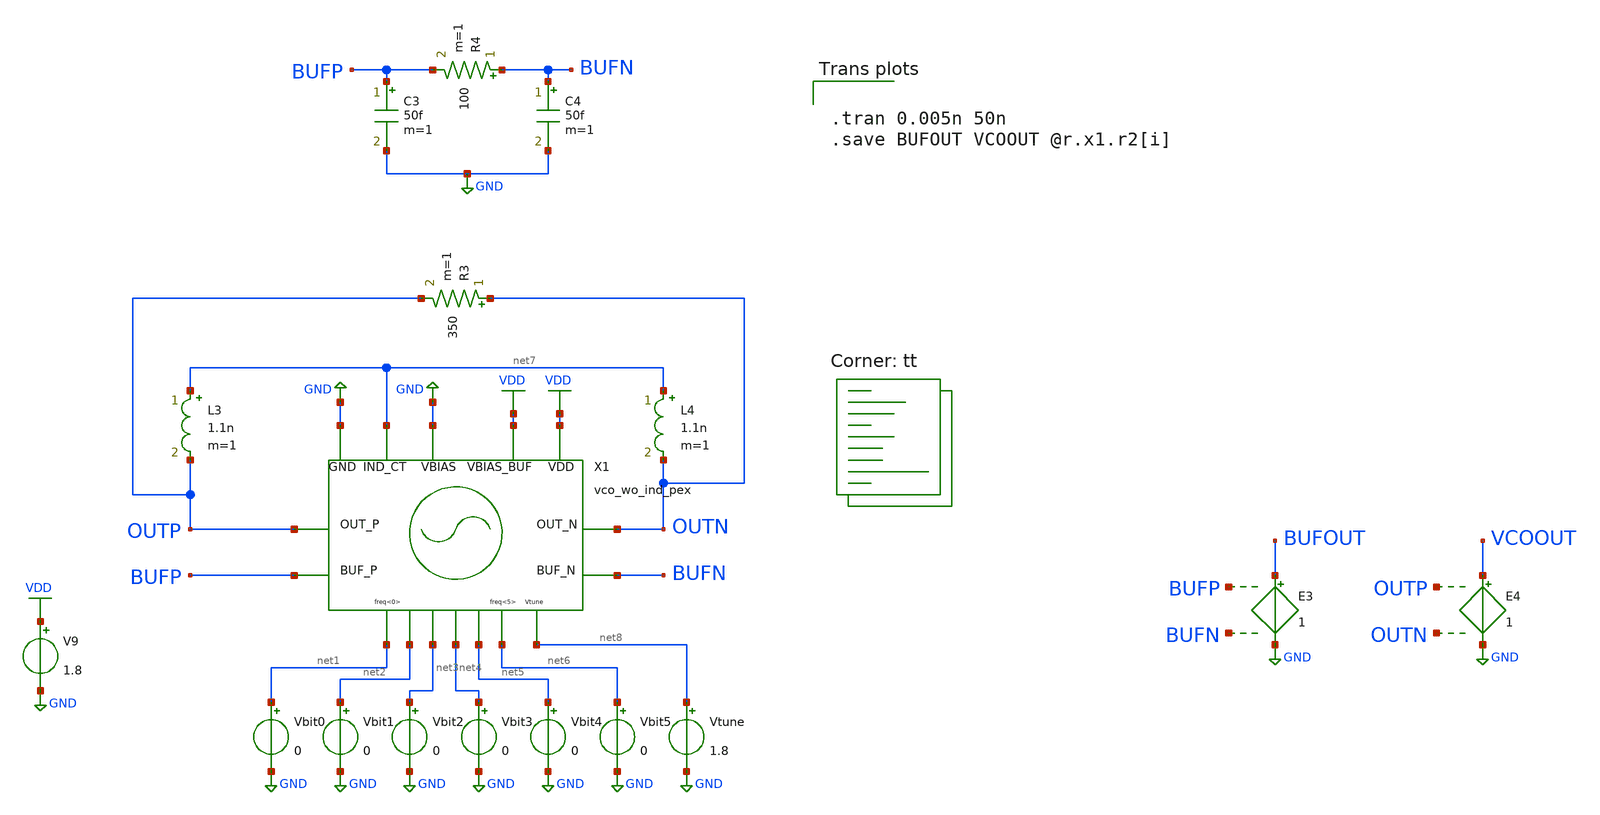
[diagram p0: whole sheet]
** sch_path: xschem/vco/testbenches/top/pex/vco_wo_ind_pex_tb.sch
* YI/C9Shc8z/CWPKLJb8BQD+O4ziO4wpAwbu7u7s7HEAy2IIt2IIlQD6O4ziO4ypAAICtDl/GPL8AgNZy7Go7vwAAAAAAAAAAAAAAAAAAAAAAAPeMn2NHvywNosQhFFq
**.subckt vco_wo_ind_pex_tb
X1 OUTP GND net7 VDD OUTN net1 net2 net3 net4 net5 net6 GND net8 BUFP BUFN VDD vco_wo_ind_pex
V9 VDD GND 1.8
Vbit0 net1 GND 0
Vbit1 net2 GND 0
Vbit2 net3 GND 0
Vbit3 net4 GND 0
Vbit4 net5 GND 0
Vbit5 net6 GND 0
L3 net7 OUTP 1.1n m=1
L4 net7 OUTN 1.1n m=1
Vtune net8 GND 1.8
R3 OUTN OUTP 350 m=1
R4 BUFN BUFP 100 m=1
C3 BUFP GND 50f m=1
C4 BUFN GND 50f m=1
E3 BUFOUT GND BUFP BUFN 1
E4 VCOOUT GND OUTP OUTN 1
**** begin user architecture code


.tran 0.005n 50n
.save BUFOUT VCOOUT @r.x1.r2[i]


.lib $::SKYWATER_MODELS/sky130.lib.spice tt
**** end user architecture code
**.ends
.GLOBAL GND
.GLOBAL VDD
.end
